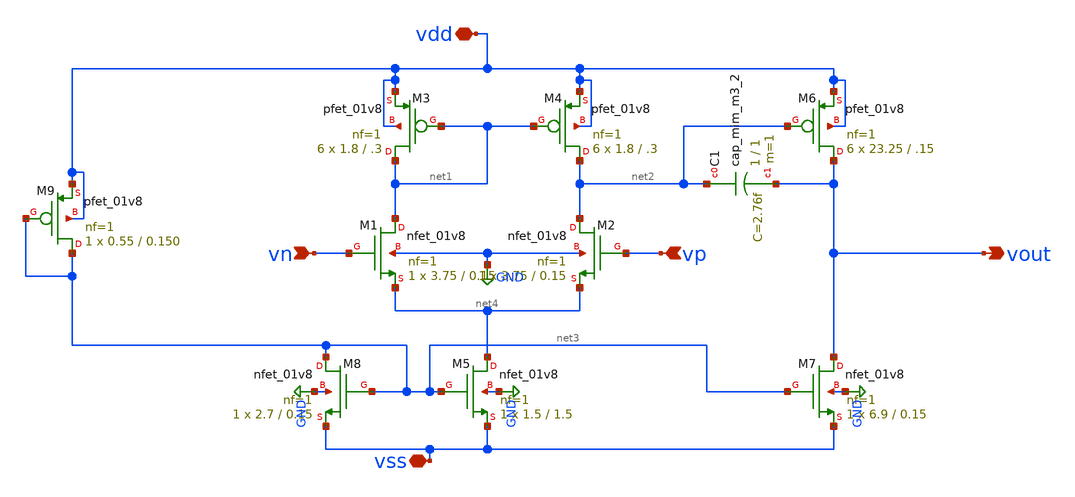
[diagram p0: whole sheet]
** sch_path: designs/subcells/core_ota_2stage/ota_2_stage.sch
**.subckt ota_2_stage vdd vp vout vn vss
*.iopin vdd
*.ipin vp
*.opin vout
*.ipin vn
*.iopin vss
XM1 net1 vn net4 GND sky130_fd_pr__nfet_01v8 L=0.15 W=3.75 nf=1 ad='int((1 + 1)/2) * 3.75 / 1 * 0.29'
+ as='int((1 + 2)/2) * 3.75 / 1 * 0.29' pd='2*int((1 + 1)/2) * (3.75 / 1 + 0.29)' ps='2*int((1 + 2)/2) * (3.75 / 1 + 0.29)'
+ nrd='0.29 / 3.75 ' nrs='0.29 / 3.75 ' sa=0 sb=0 sd=0 mult=1 m=1
XM3 net1 net1 vdd vdd sky130_fd_pr__pfet_01v8 L=.3 W=1.8 nf=1 ad='int((nf+1)/2) * W/nf * 0.29' as='int((nf+2)/2) * W/nf * 0.29'
+ pd='2*int((nf+1)/2) * (W/nf + 0.29)' ps='2*int((nf+2)/2) * (W/nf + 0.29)' nrd='0.29 / W' nrs='0.29 / W'
+ sa=0 sb=0 sd=0 mult=6 m=6
XM4 net2 net1 vdd vdd sky130_fd_pr__pfet_01v8 L=.3 W=1.8 nf=1 ad='int((nf+1)/2) * W/nf * 0.29' as='int((nf+2)/2) * W/nf * 0.29'
+ pd='2*int((nf+1)/2) * (W/nf + 0.29)' ps='2*int((nf+2)/2) * (W/nf + 0.29)' nrd='0.29 / W' nrs='0.29 / W'
+ sa=0 sb=0 sd=0 mult=6 m=6
XM2 net2 vp net4 GND sky130_fd_pr__nfet_01v8 L=0.15 W=3.75 nf=1 ad='int((1 + 1)/2) * 3.75 / 1 * 0.29'
+ as='int((1 + 2)/2) * 3.75 / 1 * 0.29' pd='2*int((1 + 1)/2) * (3.75 / 1 + 0.29)' ps='2*int((1 + 2)/2) * (3.75 / 1 + 0.29)'
+ nrd='0.29 / 3.75 ' nrs='0.29 / 3.75 ' sa=0 sb=0 sd=0 mult=1 m=1
XM5 net4 net3 vss GND sky130_fd_pr__nfet_01v8 L=1.5 W=1.5 nf=1 ad='int((1 + 1)/2) * 1.5 / 1 * 0.29' as='int((1 + 2)/2) * 1.5 / 1 * 0.29'
+ pd='2*int((1 + 1)/2) * (1.5 / 1 + 0.29)' ps='2*int((1 + 2)/2) * (1.5 / 1 + 0.29)' nrd='0.29 / 1.5 ' nrs='0.29 / 1.5 '
+ sa=0 sb=0 sd=0 mult=1 m=1
XM8 net3 net3 vss GND sky130_fd_pr__nfet_01v8 L=0.15 W=2.7 nf=1 ad='int((1 + 1)/2) * 2.7 / 1 * 0.29'
+ as='int((1 + 2)/2) * 2.7 / 1 * 0.29' pd='2*int((1 + 1)/2) * (2.7 / 1 + 0.29)' ps='2*int((1 + 2)/2) * (2.7 / 1 + 0.29)'
+ nrd='0.29 / 2.7 ' nrs='0.29 / 2.7 ' sa=0 sb=0 sd=0 mult=1 m=1
XM6 vout net2 vdd vdd sky130_fd_pr__pfet_01v8 L=.15 W=23.25 nf=1 ad='int((nf+1)/2) * W/nf * 0.29' as='int((nf+2)/2) * W/nf * 0.29'
+ pd='2*int((nf+1)/2) * (W/nf + 0.29)' ps='2*int((nf+2)/2) * (W/nf + 0.29)' nrd='0.29 / W' nrs='0.29 / W'
+ sa=0 sb=0 sd=0 mult=6 m=6
XM7 vout net3 vss GND sky130_fd_pr__nfet_01v8 L=0.15 W=6.9 nf=1 ad='int((1 + 1)/2) * 6.9 / 1 * 0.29'
+ as='int((1 + 2)/2) * 6.9 / 1 * 0.29' pd='2*int((1 + 1)/2) * (6.9 / 1 + 0.29)' ps='2*int((1 + 2)/2) * (6.9 / 1 + 0.29)'
+ nrd='0.29 / 6.9 ' nrs='0.29 / 6.9 ' sa=0 sb=0 sd=0 mult=1 m=1
XM9 net3 net3 vdd vdd sky130_fd_pr__pfet_01v8 L=0.150 W=0.55 nf=1 ad='int((nf+1)/2) * W/nf * 0.29' as='int((nf+2)/2) * W/nf * 0.29'
+ pd='2*int((nf+1)/2) * (W/nf + 0.29)' ps='2*int((nf+2)/2) * (W/nf + 0.29)' nrd='0.29 / W' nrs='0.29 / W'
+ sa=0 sb=0 sd=0 mult=1 m=1
XC1 net2 vout sky130_fd_pr__cap_mim_m3_2 W=1 L=1 MF=1 m=1
**.ends
.GLOBAL GND
.end
